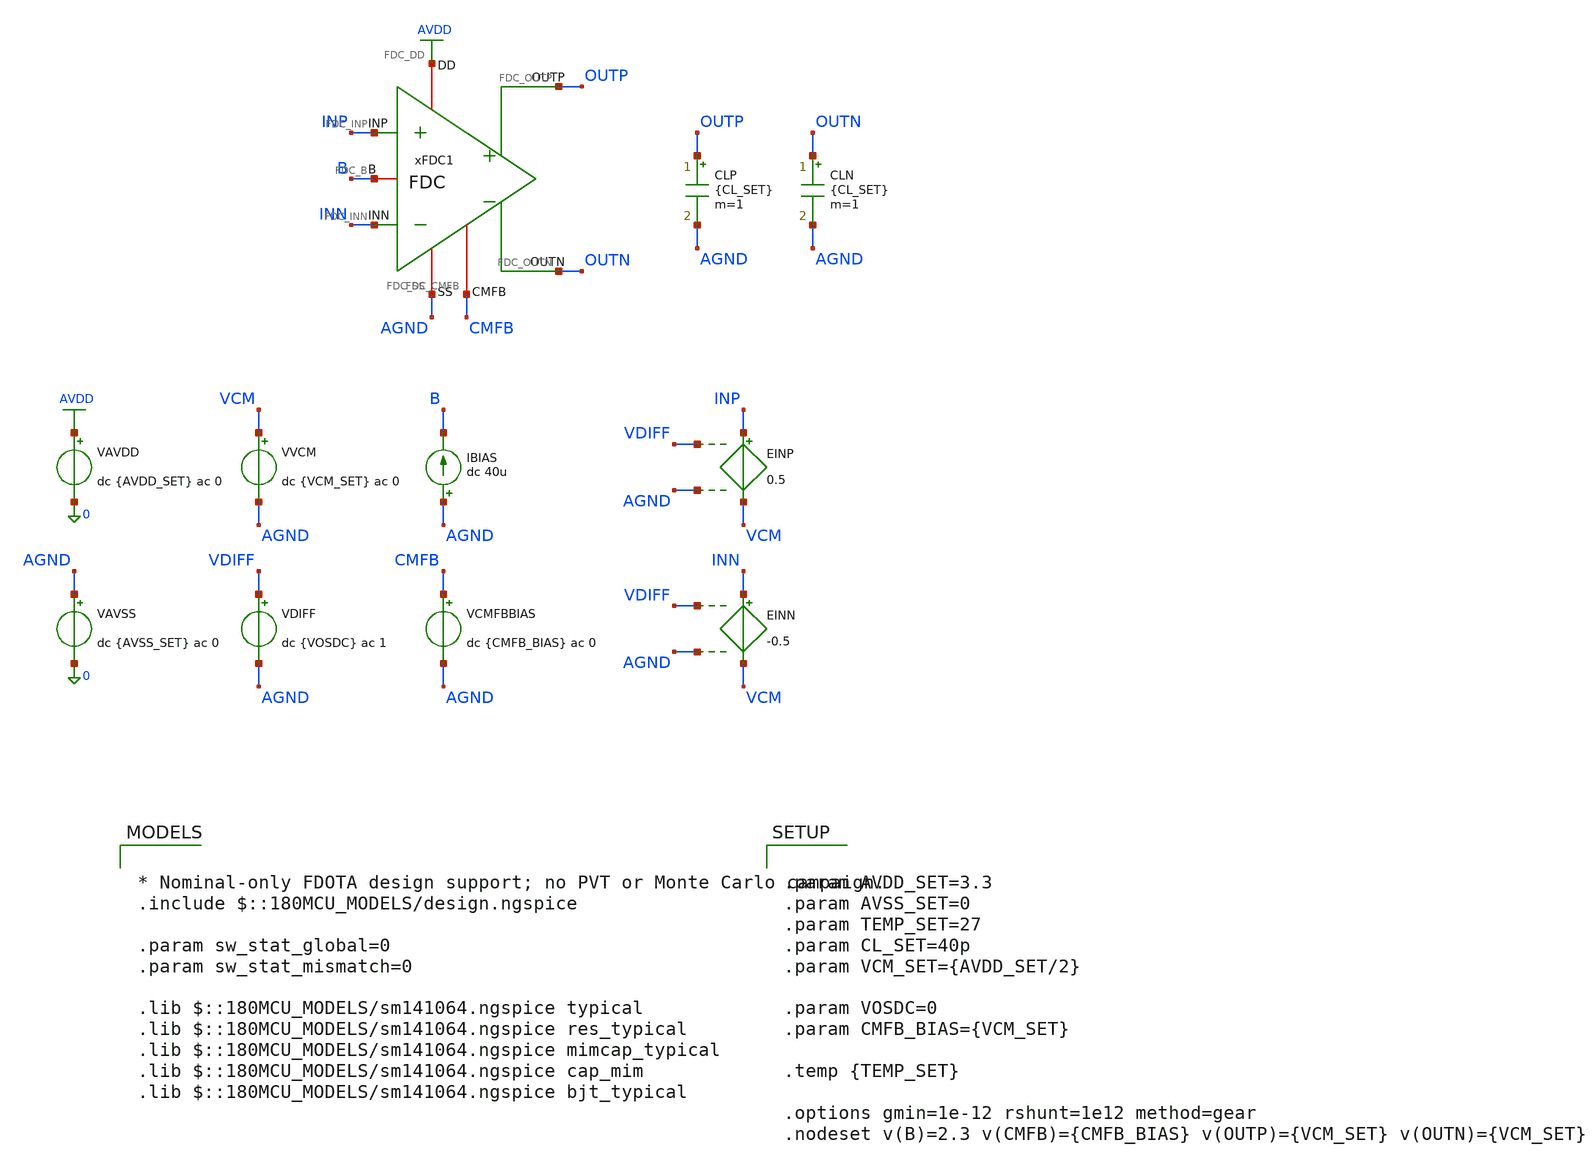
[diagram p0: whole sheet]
** sch_path: Design_Files/IC Design/Testbench/ANALOG_BLOCKS/FDOTA/FDC/FDC_TB_VCMFB_SWEEP.sch
**.subckt FDC_TB_VCMFB_SWEEP
IBIAS AGND B dc 40u
VAVDD AVDD 0 dc {AVDD_SET} ac 0
.save i(vavdd)
CLP OUTP AGND {CL_SET} m=1
VVCM VCM AGND dc {VCM_SET} ac 0
VDIFF VDIFF AGND dc {VOSDC} ac 1
VAVSS AGND 0 dc {AVSS_SET} ac 0
.save i(vavss)
EINN INN VCM VDIFF AGND -0.5
EINP INP VCM VDIFF AGND 0.5
CLN OUTN AGND {CL_SET} m=1
VCMFBBIAS CMFB AGND dc {CMFB_BIAS} ac 0
xFDC1 AVDD AGND INP INN OUTN B OUTP CMFB FDC
**** begin user architecture code

* Nominal-only FDOTA design support; no PVT or Monte Carlo campaign.
.include $::180MCU_MODELS/design.ngspice

.param sw_stat_global=0
.param sw_stat_mismatch=0

.lib $::180MCU_MODELS/sm141064.ngspice typical
.lib $::180MCU_MODELS/sm141064.ngspice res_typical
.lib $::180MCU_MODELS/sm141064.ngspice mimcap_typical
.lib $::180MCU_MODELS/sm141064.ngspice cap_mim
.lib $::180MCU_MODELS/sm141064.ngspice bjt_typical




.control
destroy all
save all
set noaskquit
set wr_vecnames
set wr_singlescale
option numdgt=15

shell mkdir -p
+ /foss/designs/ECG_Acquisition_IC/Measurement_Results/IC_Simulation/ANALOG_BLOCKS/FDOTA/FDC/Result_txt

shell rm -f
+ /foss/designs/ECG_Acquisition_IC/Measurement_Results/IC_Simulation/ANALOG_BLOCKS/FDOTA/FDC/Result_txt/vcmfb_sweep.txt

let avdd_run = 3.3
let vcm_run  = avdd_run/2
let vos_run  = 0

alter @VAVDD[DC] = $&avdd_run
alter @VVCM[DC]  = $&vcm_run
alter @VDIFF[DC] = $&vos_run

alter @VVCM[ACMAG]  = 0
alter @VDIFF[ACMAG] = 0
alter @VAVDD[ACMAG] = 0
alter @VAVSS[ACMAG] = 0

* VCMFB sweep
dc VCMFBBIAS 0 $&avdd_run 1e-4

let sweep_vcmfb  = v(cmfb)-v(agnd)
let sweep_voutp  = v(outp)-v(agnd)
let sweep_voutn  = v(outn)-v(agnd)
let sweep_voutcm = (sweep_voutp+sweep_voutn)/2
let sweep_vod    = sweep_voutp-sweep_voutn

setscale sweep_vcmfb

wrdata
+ /foss/designs/ECG_Acquisition_IC/Measurement_Results/IC_Simulation/ANALOG_BLOCKS/FDOTA/FDC/Result_txt/vcmfb_sweep.txt sweep_voutp sweep_voutn sweep_voutcm sweep_vod

quit
.endc




.param AVDD_SET=3.3
.param AVSS_SET=0
.param TEMP_SET=27
.param CL_SET=40p
.param VCM_SET={AVDD_SET/2}

.param VOSDC=0
.param CMFB_BIAS={VCM_SET}

.temp {TEMP_SET}

.options gmin=1e-12 rshunt=1e12 method=gear
.nodeset v(B)=2.3 v(CMFB)={CMFB_BIAS} v(OUTP)={VCM_SET} v(OUTN)={VCM_SET}


**** end user architecture code
**.ends
.GLOBAL AVDD
.end
